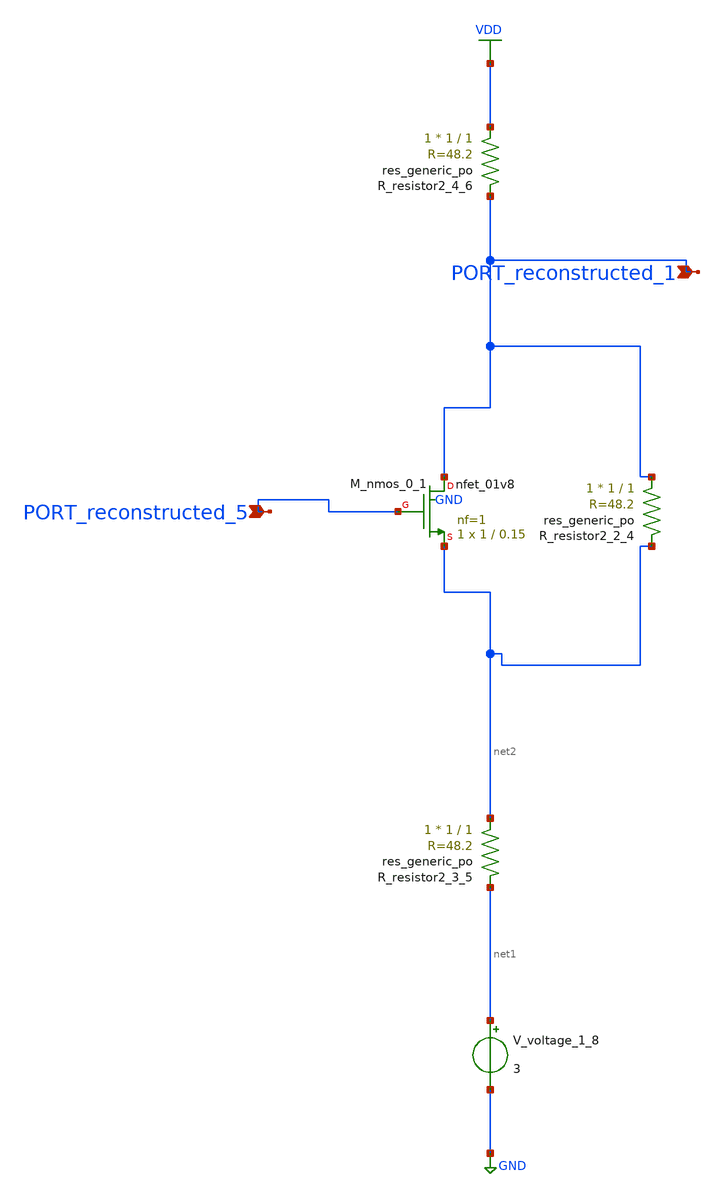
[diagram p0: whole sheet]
** sch_path: schematics/AMSNet/114.sch
**.subckt 114 PORT_reconstructed_5 PORT_reconstructed_1
*.ipin PORT_reconstructed_5
*.ipin PORT_reconstructed_1
XM_nmos_0_1 PORT_reconstructed_1 PORT_reconstructed_5 net2 GND sky130_fd_pr__nfet_01v8 L=0.15 W=1 nf=1
+ ad='int((1 + 1)/2) * 1 / 1 * 0.29' as='int((1 + 2)/2) * 1 / 1 * 0.29' pd='2*int((1 + 1)/2) * (1 / 1 + 0.29)'
+ ps='2*int((1 + 2)/2) * (1 / 1 + 0.29)' nrd='0.29 / 1 ' nrs='0.29 / 1 ' sa=0 sb=0 sd=0 mult=1 m=1
XR_resistor2_2_4 PORT_reconstructed_1 net2 sky130_fd_pr__res_generic_po W=1 L=1 m=1
XR_resistor2_3_5 net2 net1 sky130_fd_pr__res_generic_po W=1 L=1 m=1
XR_resistor2_4_6 VDD PORT_reconstructed_1 sky130_fd_pr__res_generic_po W=1 L=1 m=1
V_voltage_1_8 net1 GND 3
**.ends
.GLOBAL GND
.GLOBAL VDD
.end
